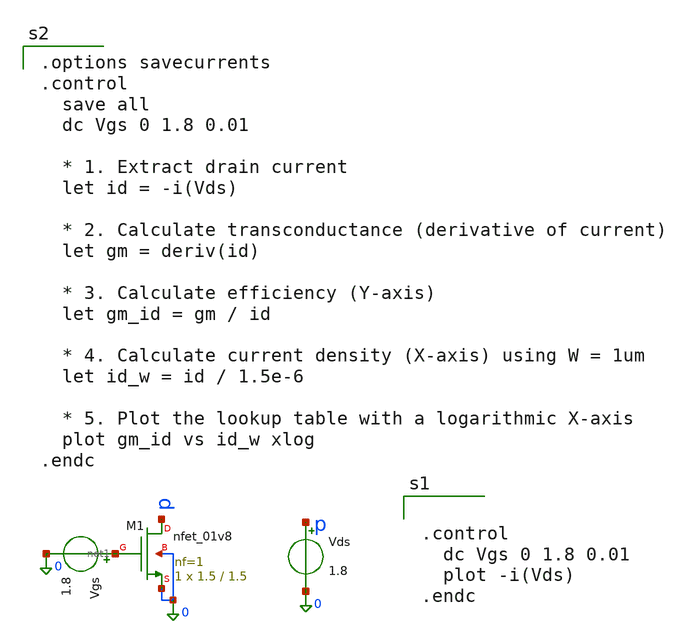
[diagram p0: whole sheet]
** sch_path: characterization/nmos_playground.sch
**.subckt nmos_playground
XM1 p net1 0 0 sky130_fd_pr__nfet_01v8 L=1.5 W=1.5 nf=1 ad='int((1 + 1)/2) * 1.5 / 1 * 0.29' as='int((1 + 2)/2) * 1.5 / 1 * 0.29'
+ pd='2*int((1 + 1)/2) * (1.5 / 1 + 0.29)' ps='2*int((1 + 2)/2) * (1.5 / 1 + 0.29)' nrd='0.29 / 1.5 ' nrs='0.29 / 1.5 '
+ sa=0 sb=0 sd=0 mult=1 m=1
Vds p 0 1.8
Vgs net1 0 1.8
**** begin user architecture code

** opencircuitdesign pdks install
.lib $::SKYWATER_MODELS/sky130.lib.spice tt


.options savecurrents
.control
  save all
  dc Vgs 0 1.8 0.01

  * 1. Extract drain current
  let id = -i(Vds)

  * 2. Calculate transconductance (derivative of current)
  let gm = deriv(id)

  * 3. Calculate efficiency (Y-axis)
  let gm_id = gm / id

  * 4. Calculate current density (X-axis) using W = 1um
  let id_w = id / 1.5e-6

  * 5. Plot the lookup table with a logarithmic X-axis
  plot gm_id vs id_w xlog
.endc



.control
  dc Vgs 0 1.8 0.01
  plot -i(Vds)
.endc

**** end user architecture code
**.ends
.end
